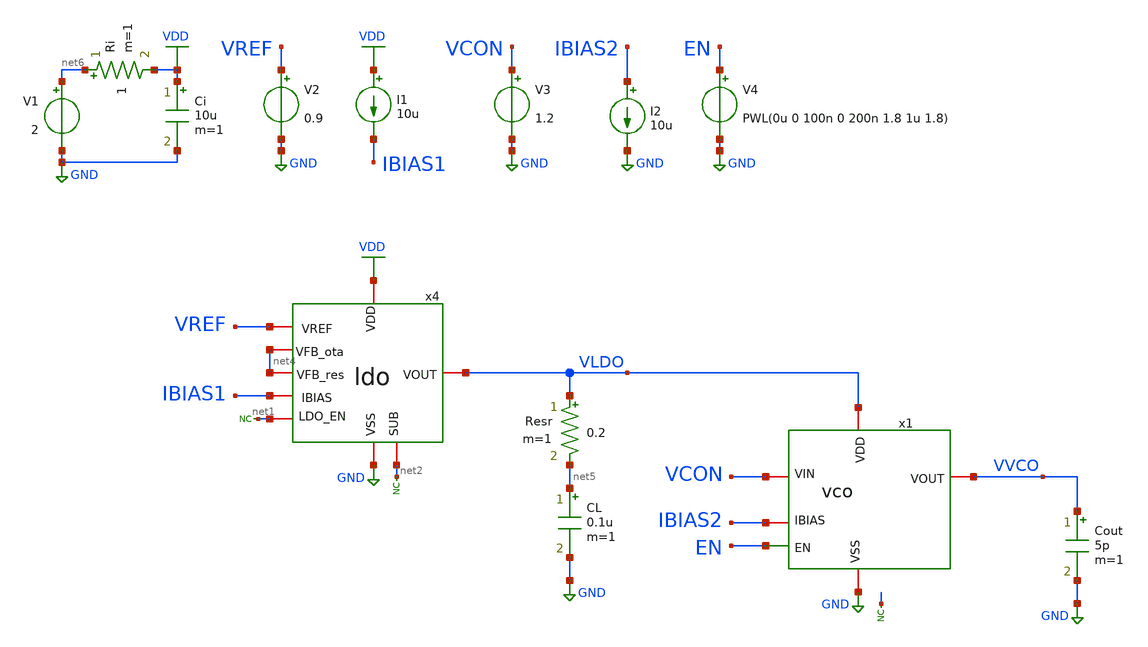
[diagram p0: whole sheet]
** sch_path: designs/libs/tb_top/tb_top/tb_top_ldo_vco/tb_top_ldo_vco.sch
**.subckt tb_top_ldo_vco
V3 VCON GND 1.2
I2 IBIAS2 GND 10u
V4 EN GND PWL(0u 0 100n 0 200n 1.8 1u 1.8)
x1 VLDO IBIAS2 VVCO EN GND VCON vco
x4 VDD VREF VLDO IBIAS1 net2 GND net1 net4 net4 ldo
* noconn #net1
* noconn #net2
* noconn #net3
V2 VREF GND 0.9
CL net5 GND 0.1u m=1
Resr VLDO net5 0.2 m=1
I1 VDD IBIAS1 10u
Ri net6 VDD 1 m=1
Ci VDD GND 10u m=1
V1 net6 GND 2
Cout VVCO GND 5p m=1
**** begin user architecture code



.control
save all

run
set color0 = white

** Simulations Temperature and Line Regulation
dc TEMP -40 125 1  V1 2 5 0.05

** Measurements
meas dc Vldo_max MAX v(VLDO)
meas dc Vldo_min MIN v(VLDO)
let dev_max = abs(Vldo_max - 1.8)
print dev_max
let dev_min = abs(Vldo_min - 1.8)
print dev_min
let Vldo_acc_abs = max(dev_max, dev_min)
print Vldo_acc_abs
let Vldo_acc_rel = (Vldo_acc_abs / 1.8) * 100
print Vldo_acc_rel

** Plots
setplot dc1
let vldo=v(VLDO)
plot vldo



write tb_top_ldo_vco.raw

.endc
* ngspice commands




.include $::180MCU_MODELS/design.ngspice
.lib $::180MCU_MODELS/sm141064.ngspice typical
.lib $::180MCU_MODELS/sm141064.ngspice cap_mim
.lib $::180MCU_MODELS/sm141064.ngspice moscap_typical
.lib $::180MCU_MODELS/sm141064.ngspice mimcap_typical
.lib $::180MCU_MODELS/sm141064.ngspice res_typical
* .lib $::180MCU_MODELS/sm141064.ngspice res_statistical
* ngspice commands

**** end user architecture code
**.ends
.GLOBAL GND
.GLOBAL VDD
.end
